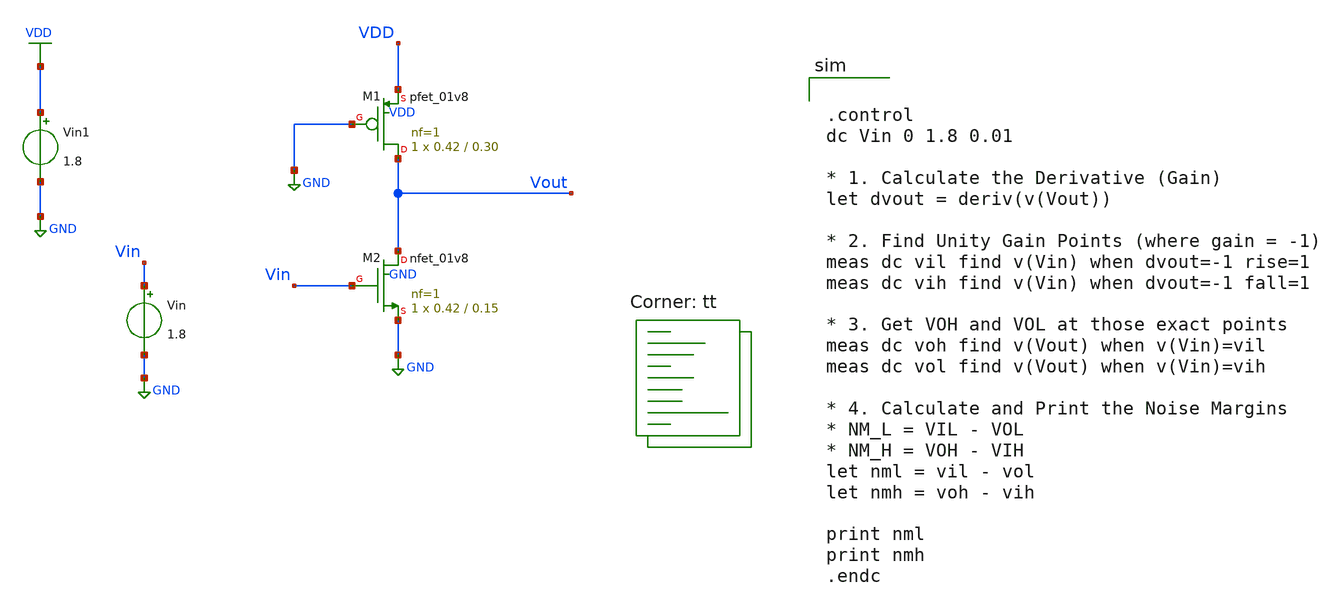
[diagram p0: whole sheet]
** sch_path: assignments/assignment2/assign2b.sch
**.subckt assign2b
XM1 Vout GND VDD VDD sky130_fd_pr__pfet_01v8 L=0.30 W=0.42 nf=1 ad='int((nf+1)/2) * W/nf * 0.29' as='int((nf+2)/2) * W/nf * 0.29'
+ pd='2*int((nf+1)/2) * (W/nf + 0.29)' ps='2*int((nf+2)/2) * (W/nf + 0.29)' nrd='0.29 / W' nrs='0.29 / W'
+ sa=0 sb=0 sd=0 mult=1 m=1
XM2 Vout Vin GND GND sky130_fd_pr__nfet_01v8 L=0.15 W=0.42 nf=1 ad='int((nf+1)/2) * W/nf * 0.29' as='int((nf+2)/2) * W/nf * 0.29'
+ pd='2*int((nf+1)/2) * (W/nf + 0.29)' ps='2*int((nf+2)/2) * (W/nf + 0.29)' nrd='0.29 / W' nrs='0.29 / W'
+ sa=0 sb=0 sd=0 mult=1 m=1
Vin1 VDD GND 1.8
Vin Vin GND 1.8
**** begin user architecture code


.control
dc Vin 0 1.8 0.01

* 1. Calculate the Derivative (Gain)
let dvout = deriv(v(Vout))

* 2. Find Unity Gain Points (where gain = -1)
meas dc vil find v(Vin) when dvout=-1 rise=1
meas dc vih find v(Vin) when dvout=-1 fall=1

* 3. Get VOH and VOL at those exact points
meas dc voh find v(Vout) when v(Vin)=vil
meas dc vol find v(Vout) when v(Vin)=vih

* 4. Calculate and Print the Noise Margins
* NM_L = VIL - VOL
* NM_H = VOH - VIH
let nml = vil - vol
let nmh = voh - vih

print nml
print nmh
.endc


.lib $::SKYWATER_MODELS/sky130.lib.spice tt
**** end user architecture code
**.ends
.GLOBAL GND
.GLOBAL VDD
.end
